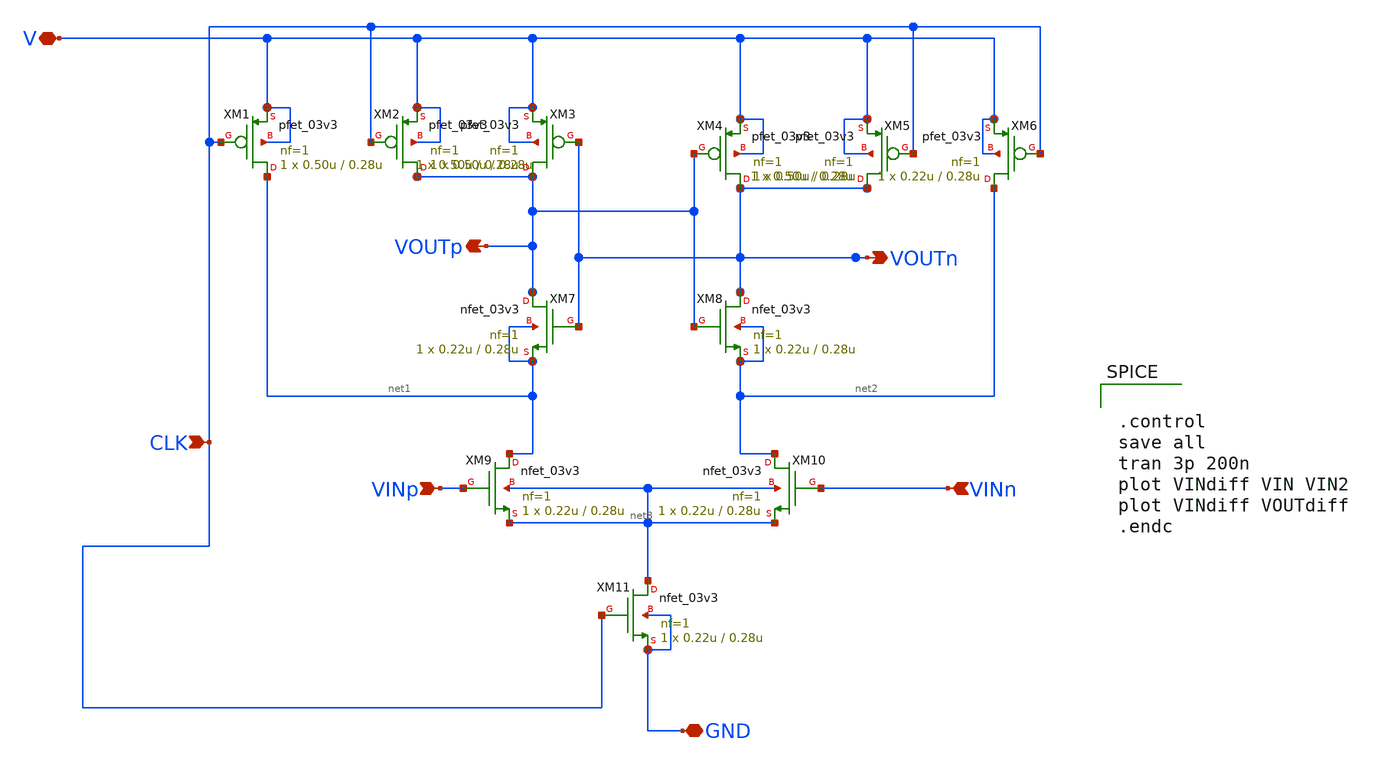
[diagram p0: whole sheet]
** sch_path: old/StrongARM.sch
**.subckt StrongARM VINp VINn CLK GND V VOUTn VOUTp
*.ipin VINp
*.ipin VINn
*.ipin CLK
*.iopin GND
*.iopin V
*.opin VOUTn
*.opin VOUTp
XM1 net1 CLK V V pfet_03v3 L=0.28u W=0.50u nf=1 ad='int((nf+1)/2) * W/nf * 0.18u' as='int((nf+2)/2) * W/nf * 0.18u'
+ pd='2*int((nf+1)/2) * (W/nf + 0.18u)' ps='2*int((nf+2)/2) * (W/nf + 0.18u)' nrd='0.18u / W' nrs='0.18u / W'
+ sa=0 sb=0 sd=0 m=1
XM2 VOUTp CLK V V pfet_03v3 L=0.28u W=0.50u nf=1 ad='int((nf+1)/2) * W/nf * 0.18u' as='int((nf+2)/2) * W/nf * 0.18u'
+ pd='2*int((nf+1)/2) * (W/nf + 0.18u)' ps='2*int((nf+2)/2) * (W/nf + 0.18u)' nrd='0.18u / W' nrs='0.18u / W'
+ sa=0 sb=0 sd=0 m=1
XM3 VOUTp VOUTn V V pfet_03v3 L=0.28u W=0.50u nf=1 ad='int((nf+1)/2) * W/nf * 0.18u' as='int((nf+2)/2) * W/nf * 0.18u'
+ pd='2*int((nf+1)/2) * (W/nf + 0.18u)' ps='2*int((nf+2)/2) * (W/nf + 0.18u)' nrd='0.18u / W' nrs='0.18u / W'
+ sa=0 sb=0 sd=0 m=1
XM4 VOUTn VOUTp V V pfet_03v3 L=0.28u W=0.50u nf=1 ad='int((nf+1)/2) * W/nf * 0.18u' as='int((nf+2)/2) * W/nf * 0.18u'
+ pd='2*int((nf+1)/2) * (W/nf + 0.18u)' ps='2*int((nf+2)/2) * (W/nf + 0.18u)' nrd='0.18u / W' nrs='0.18u / W'
+ sa=0 sb=0 sd=0 m=1
XM5 VOUTn CLK V V pfet_03v3 L=0.28u W=0.50u nf=1 ad='int((nf+1)/2) * W/nf * 0.18u' as='int((nf+2)/2) * W/nf * 0.18u'
+ pd='2*int((nf+1)/2) * (W/nf + 0.18u)' ps='2*int((nf+2)/2) * (W/nf + 0.18u)' nrd='0.18u / W' nrs='0.18u / W'
+ sa=0 sb=0 sd=0 m=1
XM6 net2 CLK V V pfet_03v3 L=0.28u W=0.22u nf=1 ad='int((nf+1)/2) * W/nf * 0.18u' as='int((nf+2)/2) * W/nf * 0.18u'
+ pd='2*int((nf+1)/2) * (W/nf + 0.18u)' ps='2*int((nf+2)/2) * (W/nf + 0.18u)' nrd='0.18u / W' nrs='0.18u / W'
+ sa=0 sb=0 sd=0 m=1
XM7 VOUTp VOUTn net1 net1 nfet_03v3 L=0.28u W=0.22u nf=1 ad='int((nf+1)/2) * W/nf * 0.18u' as='int((nf+2)/2) * W/nf * 0.18u'
+ pd='2*int((nf+1)/2) * (W/nf + 0.18u)' ps='2*int((nf+2)/2) * (W/nf + 0.18u)' nrd='0.18u / W' nrs='0.18u / W'
+ sa=0 sb=0 sd=0 m=1
XM8 VOUTn VOUTp net2 net2 nfet_03v3 L=0.28u W=0.22u nf=1 ad='int((nf+1)/2) * W/nf * 0.18u' as='int((nf+2)/2) * W/nf * 0.18u'
+ pd='2*int((nf+1)/2) * (W/nf + 0.18u)' ps='2*int((nf+2)/2) * (W/nf + 0.18u)' nrd='0.18u / W' nrs='0.18u / W'
+ sa=0 sb=0 sd=0 m=1
XM9 net1 VINp net3 net3 nfet_03v3 L=0.28u W=0.22u nf=1 ad='int((nf+1)/2) * W/nf * 0.18u' as='int((nf+2)/2) * W/nf * 0.18u'
+ pd='2*int((nf+1)/2) * (W/nf + 0.18u)' ps='2*int((nf+2)/2) * (W/nf + 0.18u)' nrd='0.18u / W' nrs='0.18u / W'
+ sa=0 sb=0 sd=0 m=1
XM10 net2 VINn net3 net3 nfet_03v3 L=0.28u W=0.22u nf=1 ad='int((nf+1)/2) * W/nf * 0.18u' as='int((nf+2)/2) * W/nf * 0.18u'
+ pd='2*int((nf+1)/2) * (W/nf + 0.18u)' ps='2*int((nf+2)/2) * (W/nf + 0.18u)' nrd='0.18u / W' nrs='0.18u / W'
+ sa=0 sb=0 sd=0 m=1
XM11 net3 CLK GND GND nfet_03v3 L=0.28u W=0.22u nf=1 ad='int((nf+1)/2) * W/nf * 0.18u' as='int((nf+2)/2) * W/nf * 0.18u'
+ pd='2*int((nf+1)/2) * (W/nf + 0.18u)' ps='2*int((nf+2)/2) * (W/nf + 0.18u)' nrd='0.18u / W' nrs='0.18u / W'
+ sa=0 sb=0 sd=0 m=1
**** begin user architecture code


.control
save all
tran 3p 200n
plot VINdiff VIN VIN2
plot VINdiff VOUTdiff
.endc


.include /foss/pdks/gf180mcuC/libs.tech/ngspice/design.ngspice
.lib /foss/pdks/gf180mcuC/libs.tech/ngspice/sm141064.ngspice typical

**** end user architecture code
**.ends
.end
